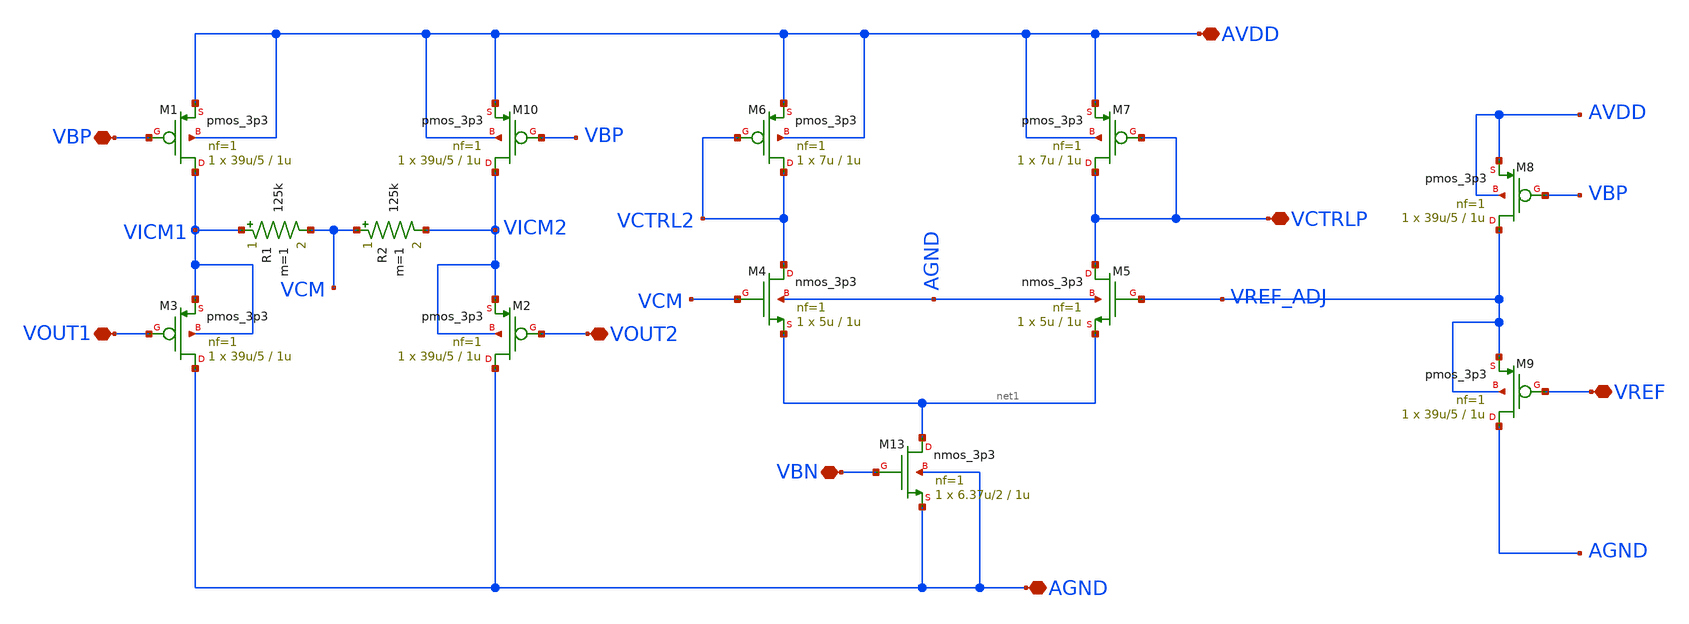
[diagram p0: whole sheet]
** sch_path: ITI_Labs/Lab11_Xschem/Design/CMFB_real.sch
**.subckt CMFB_real VOUT1 VOUT2 VCTRLP VBP AVDD AGND VBN VREF
*.iopin VOUT1
*.iopin VOUT2
*.iopin VCTRLP
*.iopin VBP
*.iopin AVDD
*.iopin AGND
*.iopin VBN
*.iopin VREF
XM4 VCTRL2 VCM net1 AGND nmos_3p3 L=1u W=5u nf=1 ad='int((nf+1)/2) * W/nf * 0.18u' as='int((nf+2)/2) * W/nf * 0.18u'
+ pd='2*int((nf+1)/2) * (W/nf + 0.18u)' ps='2*int((nf+2)/2) * (W/nf + 0.18u)' nrd='0.18u / W' nrs='0.18u / W'
+ sa=0 sb=0 sd=0 m=1
XM5 VCTRLP VREF_ADJ net1 AGND nmos_3p3 L=1u W=5u nf=1 ad='int((nf+1)/2) * W/nf * 0.18u' as='int((nf+2)/2) * W/nf * 0.18u'
+ pd='2*int((nf+1)/2) * (W/nf + 0.18u)' ps='2*int((nf+2)/2) * (W/nf + 0.18u)' nrd='0.18u / W' nrs='0.18u / W'
+ sa=0 sb=0 sd=0 m=1
XM6 VCTRL2 VCTRL2 AVDD AVDD pmos_3p3 L=1u W=7u nf=1 ad='int((nf+1)/2) * W/nf * 0.18u' as='int((nf+2)/2) * W/nf * 0.18u'
+ pd='2*int((nf+1)/2) * (W/nf + 0.18u)' ps='2*int((nf+2)/2) * (W/nf + 0.18u)' nrd='0.18u / W' nrs='0.18u / W'
+ sa=0 sb=0 sd=0 m=1
XM7 VCTRLP VCTRLP AVDD AVDD pmos_3p3 L=1u W=7u nf=1 ad='int((nf+1)/2) * W/nf * 0.18u' as='int((nf+2)/2) * W/nf * 0.18u'
+ pd='2*int((nf+1)/2) * (W/nf + 0.18u)' ps='2*int((nf+2)/2) * (W/nf + 0.18u)' nrd='0.18u / W' nrs='0.18u / W'
+ sa=0 sb=0 sd=0 m=1
R1 VICM1 VCM 125k m=1
R2 VCM VICM2 125k m=1
XM10 VICM2 VBP AVDD AVDD pmos_3p3 L=1u W=39u/5 nf=1 ad='int((nf+1)/2) * W/nf * 0.18u' as='int((nf+2)/2) * W/nf * 0.18u'
+ pd='2*int((nf+1)/2) * (W/nf + 0.18u)' ps='2*int((nf+2)/2) * (W/nf + 0.18u)' nrd='0.18u / W' nrs='0.18u / W'
+ sa=0 sb=0 sd=0 m=1
XM1 VICM1 VBP AVDD AVDD pmos_3p3 L=1u W=39u/5 nf=1 ad='int((nf+1)/2) * W/nf * 0.18u' as='int((nf+2)/2) * W/nf * 0.18u'
+ pd='2*int((nf+1)/2) * (W/nf + 0.18u)' ps='2*int((nf+2)/2) * (W/nf + 0.18u)' nrd='0.18u / W' nrs='0.18u / W'
+ sa=0 sb=0 sd=0 m=1
XM13 net1 VBN AGND AGND nmos_3p3 L=1u W=6.37u/2 nf=1 ad='int((nf+1)/2) * W/nf * 0.18u' as='int((nf+2)/2) * W/nf * 0.18u'
+ pd='2*int((nf+1)/2) * (W/nf + 0.18u)' ps='2*int((nf+2)/2) * (W/nf + 0.18u)' nrd='0.18u / W' nrs='0.18u / W'
+ sa=0 sb=0 sd=0 m=1
XM2 AGND VOUT2 VICM2 VICM2 pmos_3p3 L=1u W=39u/5 nf=1 ad='int((nf+1)/2) * W/nf * 0.18u' as='int((nf+2)/2) * W/nf * 0.18u'
+ pd='2*int((nf+1)/2) * (W/nf + 0.18u)' ps='2*int((nf+2)/2) * (W/nf + 0.18u)' nrd='0.18u / W' nrs='0.18u / W'
+ sa=0 sb=0 sd=0 m=1
XM3 AGND VOUT1 VICM1 VICM1 pmos_3p3 L=1u W=39u/5 nf=1 ad='int((nf+1)/2) * W/nf * 0.18u' as='int((nf+2)/2) * W/nf * 0.18u'
+ pd='2*int((nf+1)/2) * (W/nf + 0.18u)' ps='2*int((nf+2)/2) * (W/nf + 0.18u)' nrd='0.18u / W' nrs='0.18u / W'
+ sa=0 sb=0 sd=0 m=1
XM8 VREF_ADJ VBP AVDD AVDD pmos_3p3 L=1u W=39u/5 nf=1 ad='int((nf+1)/2) * W/nf * 0.18u' as='int((nf+2)/2) * W/nf * 0.18u'
+ pd='2*int((nf+1)/2) * (W/nf + 0.18u)' ps='2*int((nf+2)/2) * (W/nf + 0.18u)' nrd='0.18u / W' nrs='0.18u / W'
+ sa=0 sb=0 sd=0 m=1
XM9 AGND VREF VREF_ADJ VREF_ADJ pmos_3p3 L=1u W=39u/5 nf=1 ad='int((nf+1)/2) * W/nf * 0.18u' as='int((nf+2)/2) * W/nf * 0.18u'
+ pd='2*int((nf+1)/2) * (W/nf + 0.18u)' ps='2*int((nf+2)/2) * (W/nf + 0.18u)' nrd='0.18u / W' nrs='0.18u / W'
+ sa=0 sb=0 sd=0 m=1
**.ends
.end
